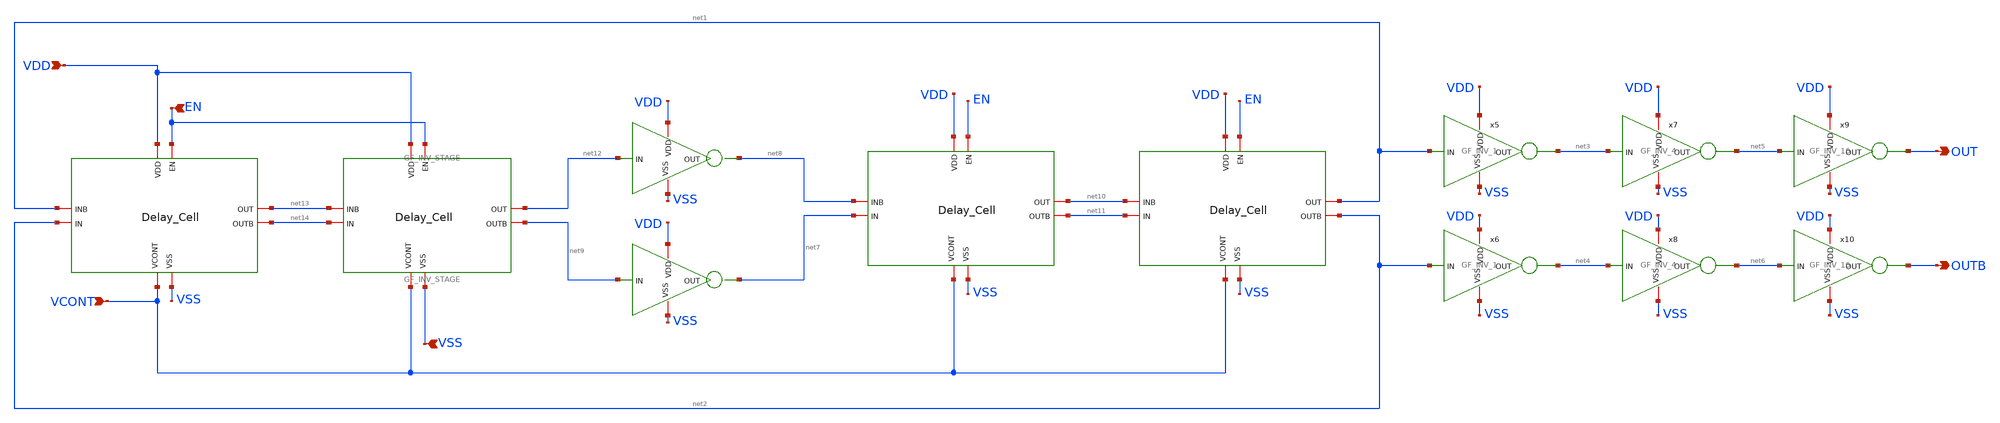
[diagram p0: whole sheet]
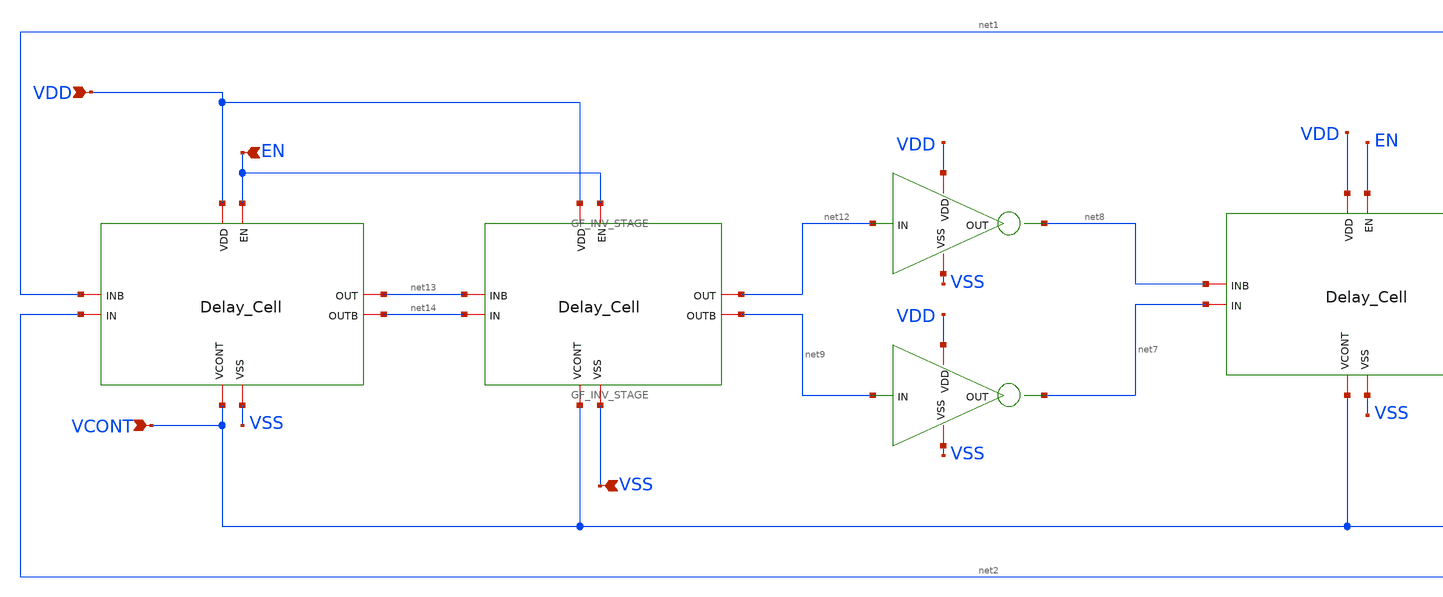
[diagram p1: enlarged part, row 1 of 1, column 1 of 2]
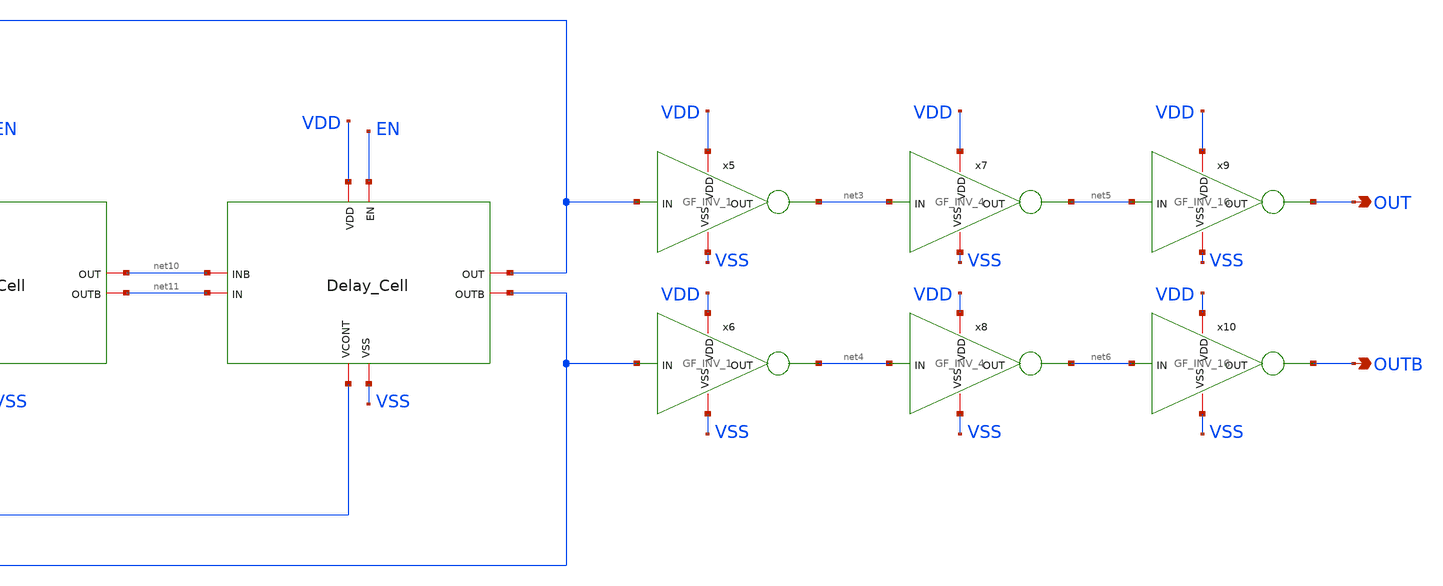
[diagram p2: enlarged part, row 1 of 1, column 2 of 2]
** sch_path: Clock_Generator_PAKISTAN_02/Schematics/VCO.sch
**.subckt VCO OUT OUTB VDD VCONT EN VSS
*.opin OUT
*.opin OUTB
*.ipin VDD
*.ipin VCONT
*.ipin EN
*.ipin VSS
x5 VSS VDD net3 net1 GF_INV_1
x6 VSS VDD net4 net2 GF_INV_1
x7 VSS VDD net5 net3 GF_INV_4
x8 VSS VDD net6 net4 GF_INV_4
x9 VSS VDD OUT net5 GF_INV_16
x10 VSS VDD OUTB net6 GF_INV_16
x3 VSS VDD net8 net12 GF_INV_STAGE
x4 VSS VDD net7 net9 GF_INV_STAGE
x1 VDD VSS VCONT net14 net13 net12 net9 EN Delay_Cell
x2 VDD VSS VCONT net7 net8 net10 net11 EN Delay_Cell
x11 VDD VSS VCONT net2 net1 net13 net14 EN Delay_Cell
x12 VDD VSS VCONT net11 net10 net1 net2 EN Delay_Cell
**.ends
.end
